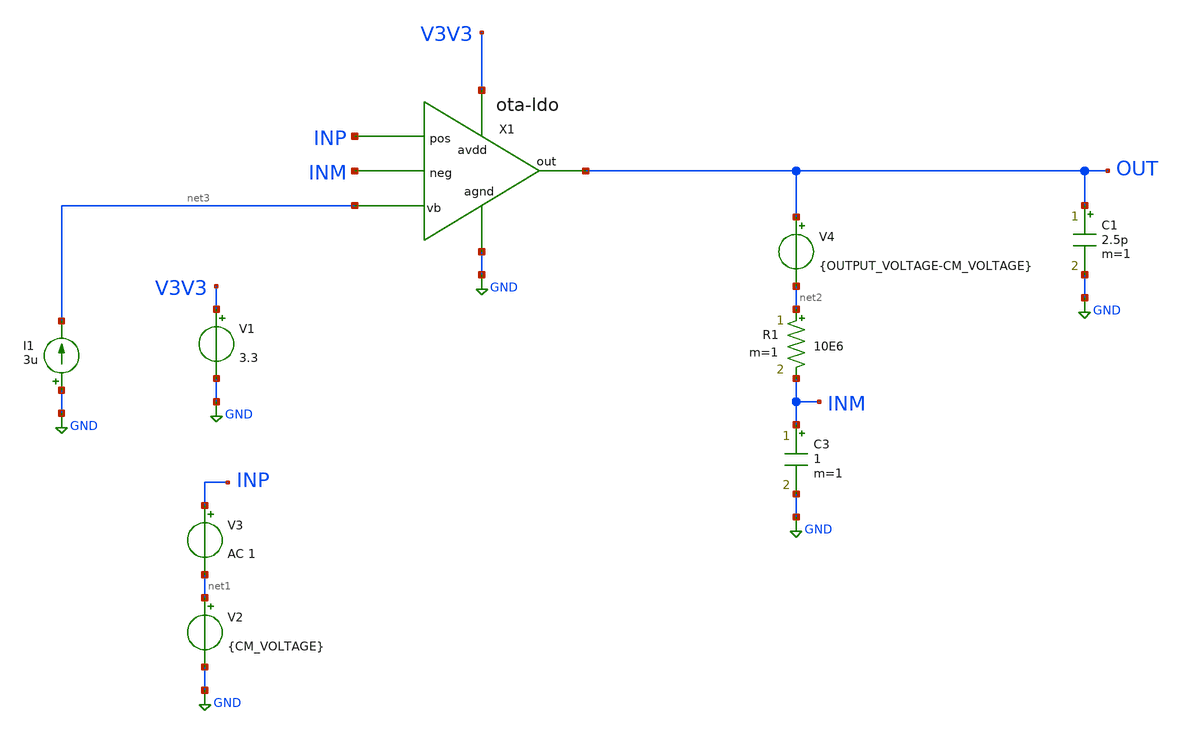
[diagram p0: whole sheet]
** sch_path: LDO/xschem/ota-ldo/test/ota-ldo-test.sch
**.subckt ota-ldo-test
V1 V3V3 GND 3.3
V2 net1 GND {CM_VOLTAGE}
V3 INP net1 AC 1
R1 net2 INM 10E6 m=1
V4 OUT net2 {OUTPUT_VOLTAGE-CM_VOLTAGE}
C3 INM GND 1 m=1
I1 GND net3 3u
X1 V3V3 OUT INM INP net3 GND ota-ldo
C1 OUT GND 2.5p m=1
**** begin user architecture code


.include $env(PDK_ROOT)/$env(PDK)/libs.tech/ngspice/design.ngspice
.lib $env(PDK_ROOT)/$env(PDK)/libs.tech/ngspice/sm141064.ngspice typical
.lib $env(PDK_ROOT)/$env(PDK)/libs.tech/ngspice/sm141064.ngspice mimcap_statistical
.lib $env(PDK_ROOT)/$env(PDK)/libs.tech/ngspice/sm141064.ngspice cap_mim

*.options savecurrents
.save all

*.lib /foss/pdks/sky130A/libs.tech/ngspice/sky130.lib.spice tt
.param CM_VOLTAGE = 0.9
.param OUTPUT_VOLTAGE = 1
.control

*save all


ac dec 200 10 1000Meg
settype decibel out
plot vdb(out)
wrdata /foss/designs/LDO_Design/data/data_OTAvoutdb.dat vdb(out)
let phase_val = 180/PI*cph(out)
let phase_margin_val = 180 + 180/PI*cph(out)
settype phase phase_val
plot phase_val
wrdata /foss/designs/LDO_Design/data/data_OTAphase_val.dat phase_val
meas ac phase_margin find phase_margin_val when vdb(out)=0
meas ac crossover_freq WHEN vdb(out)=0


let gm1  = @m.x1.xm1.m0[gm]
print gm1

*wrdata /foss/designs/IPD413_2023_HW1_git/data_nmos_gmvgs_VDSp9.dat gmn




let id1  = @m.x1.xm1.m0[gm]
*let id2  = @m.x1.xm2.msky130_fd_pr__nfet_01v8_lvt[id]
*let id3  = @m.x1.xm3.msky130_fd_pr__pfet_01v8_lvt[id]
*let id4  = @m.x1.xm4.msky130_fd_pr__pfet_01v8_lvt[id]
*let id5  = @m.x1.xm5.msky130_fd_pr__pfet_01v8_lvt[id]
*let id6  = @m.x1.xm6.msky130_fd_pr__nfet_01v8_lvt[id]
*let id7  = @m.x1.xm7.msky130_fd_pr__nfet_01v8_lvt[id]
*let id8  = @m.x1.xm8.msky130_fd_pr__nfet_01v8_lvt[id]


*let gm2  = @m.x1.xm2.msky130_fd_pr__nfet_01v8_lvt[gm]
*let gm3  = @m.x1.xm3.msky130_fd_pr__pfet_01v8_lvt[gm]
*let gm4  = @m.x1.xm4.msky130_fd_pr__pfet_01v8_lvt[gm]
let gm5  = @m.x1.xm5.m0[gm]
*let gm6  = @m.x1.xm6.msky130_fd_pr__nfet_01v8_lvt[gm]
*let gm7  = @m.x1.xm7.msky130_fd_pr__nfet_01v8_lvt[gm]
*let gm8  = @m.x1.xm8.msky130_fd_pr__nfet_01v8_lvt[gm]

let gds2 = @m.x1.xm2.m0[gds]
*plot gds
let gds4 = @m.x1.xm4.m0[gds]
let gds5 = @m.x1.xm5.m0[gds]
let gds6 = @m.x1.xm6.m0[gds]


*let vgs1  = @m.x1.xm1.msky130_fd_pr__nfet_01v8_lvt[vgs]
*let vth1  = @m.x1.xm1.msky130_fd_pr__nfet_01v8_lvt[vth]
*let vov1 = vgs1 - vth1
*let vds1  = @m.x1.xm1.msky130_fd_pr__nfet_01v8_lvt[vds]
*let vdsat1  = @m.x1.xm1.msky130_fd_pr__nfet_01v8_lvt[vdsat]

let cgs5  = @m.x1.xm5.m0[cgg]

*@m.xm1.m0[id]
*print v(inp)
*print v(inm)
*print v(out)
let v_offset = v(inp)-v(inm)
*print v_offset

print cgs5
print id1
*print id2
*print id5
*print gm1
*print gm2
*print gm5
*print id7
*print id8
print gm5
print gm1
print gm1/(gds2+gds4)
print gm5/(gds5+gds6)

*print v(vgs1)
*print v(vth1)
*print v(vov1)
*print v(vds1)
*print v(vdsat1)

write /workspaces/DC23-LTC2/LDO/xschem/ota-ldo/data all

.endc

**** end user architecture code
**.ends

* expanding   symbol:  ./ota-ldo.sym # of pins=6
** sym_path: LDO/xschem/ota-ldo/ota-ldo.sym
** sch_path: LDO/xschem/ota-ldo/ota-ldo.sch
.subckt ota-ldo avdd out neg pos vb agnd
*.iopin vb
*.iopin avdd
*.iopin agnd
*.ipin neg
*.ipin pos
*.opin out
XC2 net2 out cap_mim_1f5fF c_width=50e-6 c_length=20e-6 m=1
XM1 net1 neg net3 agnd nfet_03v3 L=0.3u W=10u nf=1 ad='int((nf+1)/2) * W/nf * 0.18u' as='int((nf+2)/2) * W/nf * 0.18u'
+ pd='2*int((nf+1)/2) * (W/nf + 0.18u)' ps='2*int((nf+2)/2) * (W/nf + 0.18u)' nrd='0.18u / W' nrs='0.18u / W'
+ sa=0 sb=0 sd=0 m=1
XM3 net1 net1 avdd avdd pfet_03v3 L=0.8u W=9u nf=1 ad='int((nf+1)/2) * W/nf * 0.18u' as='int((nf+2)/2) * W/nf * 0.18u'
+ pd='2*int((nf+1)/2) * (W/nf + 0.18u)' ps='2*int((nf+2)/2) * (W/nf + 0.18u)' nrd='0.18u / W' nrs='0.18u / W'
+ sa=0 sb=0 sd=0 m=1
XM2 net2 pos net3 agnd nfet_03v3 L=0.3u W=10u nf=1 ad='int((nf+1)/2) * W/nf * 0.18u' as='int((nf+2)/2) * W/nf * 0.18u'
+ pd='2*int((nf+1)/2) * (W/nf + 0.18u)' ps='2*int((nf+2)/2) * (W/nf + 0.18u)' nrd='0.18u / W' nrs='0.18u / W'
+ sa=0 sb=0 sd=0 m=1
XM4 net2 net1 avdd avdd pfet_03v3 L=0.8u W=9u nf=1 ad='int((nf+1)/2) * W/nf * 0.18u' as='int((nf+2)/2) * W/nf * 0.18u'
+ pd='2*int((nf+1)/2) * (W/nf + 0.18u)' ps='2*int((nf+2)/2) * (W/nf + 0.18u)' nrd='0.18u / W' nrs='0.18u / W'
+ sa=0 sb=0 sd=0 m=1
XM7 net3 vb agnd agnd nfet_03v3 L=0.8u W=16u nf=1 ad='int((nf+1)/2) * W/nf * 0.18u' as='int((nf+2)/2) * W/nf * 0.18u'
+ pd='2*int((nf+1)/2) * (W/nf + 0.18u)' ps='2*int((nf+2)/2) * (W/nf + 0.18u)' nrd='0.18u / W' nrs='0.18u / W'
+ sa=0 sb=0 sd=0 m=1
XM8 vb vb agnd agnd nfet_03v3 L=0.8u W=1.66u nf=1 ad='int((nf+1)/2) * W/nf * 0.18u' as='int((nf+2)/2) * W/nf * 0.18u'
+ pd='2*int((nf+1)/2) * (W/nf + 0.18u)' ps='2*int((nf+2)/2) * (W/nf + 0.18u)' nrd='0.18u / W' nrs='0.18u / W'
+ sa=0 sb=0 sd=0 m=1
XM5 out net2 avdd avdd pfet_03v3 L=0.4u W=60u nf=1 ad='int((nf+1)/2) * W/nf * 0.18u' as='int((nf+2)/2) * W/nf * 0.18u'
+ pd='2*int((nf+1)/2) * (W/nf + 0.18u)' ps='2*int((nf+2)/2) * (W/nf + 0.18u)' nrd='0.18u / W' nrs='0.18u / W'
+ sa=0 sb=0 sd=0 m=1
XM6 out vb agnd agnd nfet_03v3 L=0.8u W=60u nf=1 ad='int((nf+1)/2) * W/nf * 0.18u' as='int((nf+2)/2) * W/nf * 0.18u'
+ pd='2*int((nf+1)/2) * (W/nf + 0.18u)' ps='2*int((nf+2)/2) * (W/nf + 0.18u)' nrd='0.18u / W' nrs='0.18u / W'
+ sa=0 sb=0 sd=0 m=1
.ends

.GLOBAL GND
.end
